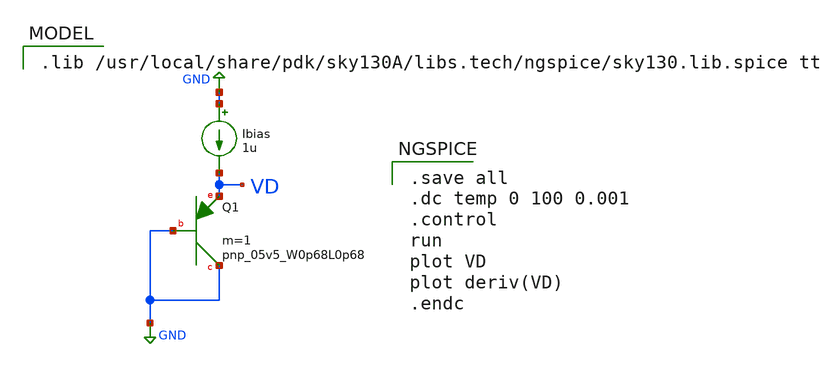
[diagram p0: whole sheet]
** sch_path: 1_diode_0p68_VD_temp.sch
**.subckt 1_diode_0p68_VD_temp
XQ1 GND GND VD sky130_fd_pr__pnp_05v5_W0p68L0p68 m=1
Ibias GND VD 1u
**** begin user architecture code

.save all
.dc temp 0 100 0.001
.control
run
plot VD
plot deriv(VD)
.endc


.lib /usr/local/share/pdk/sky130A/libs.tech/ngspice/sky130.lib.spice tt

**** end user architecture code
**.ends
.GLOBAL GND
.end
